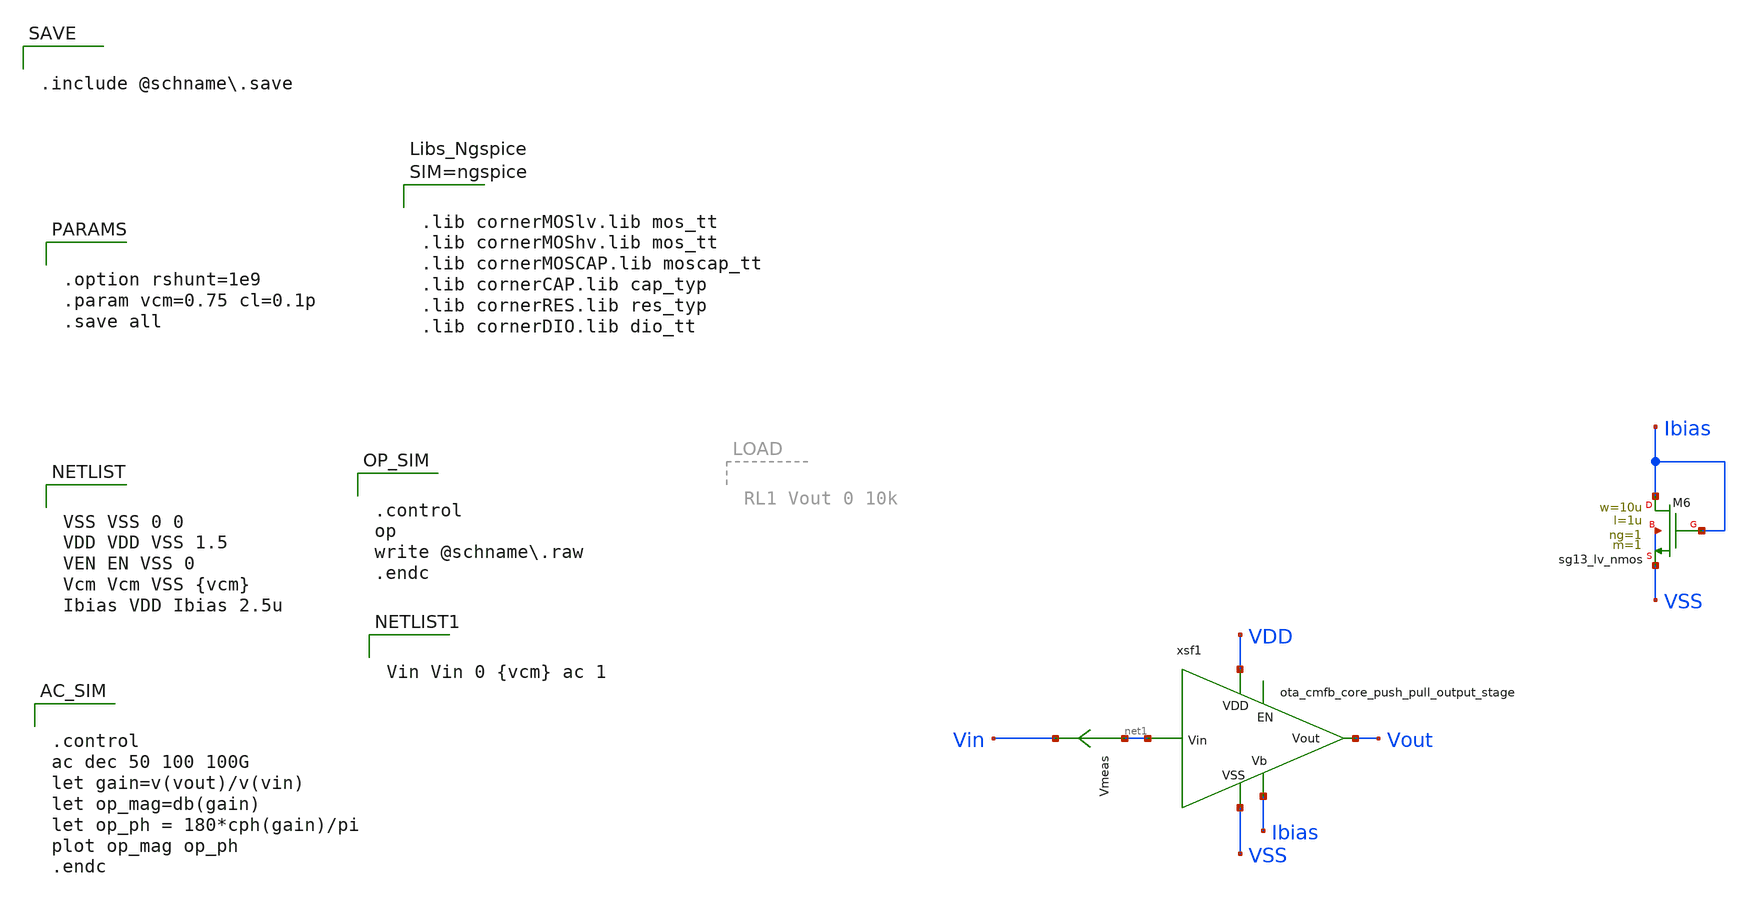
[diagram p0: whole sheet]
** sch_path: schema/ota_cmfb_core/ota_cmfb_core_push_pull_output_stage_tb.sch
**.subckt ota_cmfb_core_push_pull_output_stage_tb
XM6 Ibias Ibias VSS VSS sg13_lv_nmos w=10u l=1u ng=1 m=1 mm_ok=1
Vmeas net1 Vin 0
.save i(vmeas)
xsf1 VDD net1 Vout Ibias VSS ota_cmfb_core_push_pull_output_stage
**** begin user architecture code


VSS VSS 0 0
VDD VDD VSS 1.5
VEN EN VSS 0
Vcm Vcm VSS {vcm}
Ibias VDD Ibias 2.5u



.control
op
write @schname.raw
.endc



.control
ac dec 50 100 100G
let gain=v(vout)/v(vin)
let op_mag=db(gain)
let op_ph = 180*cph(gain)/pi
plot op_mag op_ph
.endc




.option rshunt=1e9
.param vcm=0.75 cl=0.1p
.save all



.include @schname.save



Vin Vin 0 {vcm} ac 1





.lib cornerMOSlv.lib mos_tt
.lib cornerMOShv.lib mos_tt
.lib cornerMOSCAP.lib moscap_tt
.lib cornerCAP.lib cap_typ
.lib cornerRES.lib res_typ
.lib cornerDIO.lib dio_tt



**** end user architecture code
**.ends

* expanding   symbol:
*+  /foss/designs/Chipalooza2/schema/ota_cmfb_core/ota_cmfb_core_push_pull_output_stage.sym # of pins=5
** sym_path: schema/ota_cmfb_core/ota_cmfb_core_push_pull_output_stage.sym
** sch_path: schema/ota_cmfb_core/ota_cmfb_core_push_pull_output_stage.sch
.subckt ota_cmfb_core_push_pull_output_stage VDD Vin Vout Vbias VSS
*.iopin VSS
*.iopin VDD
*.ipin Vbias
*.ipin Vin
*.opin Vout
XM1 Vout Vin_shifted VSS VSS sg13_lv_nmos w=2.5u l=0.5u ng=1 m=1 mm_ok=1
XM2 VDD Vin Vout VDD sg13_lv_pmos w=5u l=0.5u ng=1 m=1 mm_ok=1
XM5 VDD Vbiasp net2 VDD sg13_lv_pmos w=10u l=3u ng=1 m=1 mm_ok=1
XM6 net1 Vbiasn VSS VSS sg13_lv_nmos w=5u l=0.5u ng=1 m=1 mm_ok=1
XM4 Vin_shifted Vcasp2 Vin VDD sg13_lv_pmos w=5u l=3u ng=1 m=1 mm_ok=1
XM15 Vin_shifted Vcasn net1 VSS sg13_lv_nmos w=5u l=0.5u ng=1 m=1 mm_ok=1
XM16 net2 Vcasp Vin VDD sg13_lv_pmos w=10u l=3u ng=1 m=1 mm_ok=1
XM3 Vin Vcasn2 Vin_shifted VSS sg13_lv_nmos w=1.4u l=3u ng=1 m=1 mm_ok=1
XM8 VDD Vbiasp Vbiasp VDD sg13_lv_pmos w=10u l=3u ng=1 m=1 mm_ok=1
XM9 Vbiasp Vcasp Vcasp VDD sg13_lv_pmos w=10u l=3u ng=1 m=1 mm_ok=1
XM13 Vcasp Vcasp2 Vcasp2 VDD sg13_lv_pmos w=5u l=3u ng=1 m=2 mm_ok=1
XM10 VDD Vbiasp Vcasn2 VDD sg13_lv_pmos w=10u l=3u ng=1 m=1 mm_ok=1
XM11 Vcasn2 Vcasn2 Vcasn VSS sg13_lv_nmos w=1.4u l=3u ng=1 m=2 mm_ok=1
XM12 Vcasn Vcasn Vbiasn VSS sg13_lv_nmos w=5u l=0.5u ng=1 m=1 mm_ok=1
XM14 Vbiasn Vbiasn VSS VSS sg13_lv_nmos w=5u l=0.5u ng=1 m=1 mm_ok=1
XM7 Vcasp2 Vbias VSS VSS sg13_lv_nmos w=2u l=1u ng=1 m=2 mm_ok=1
XR1 net3 Vout sub! rhigh w=0.5e-6 l=1e-6 m=1 b=0 mm_ok=1
XR2 net4 Vout sub! rhigh w=0.5e-6 l=1e-6*2 m=1 b=0 mm_ok=1
XC1 net3 Vin sg13_moscap_p w=5.0u l=5.0u m=3 mm_ok=1
XC2 net4 Vin_shifted sg13_moscap_p w=5.0u l=5.0u m=3 mm_ok=1
.ends

.end
